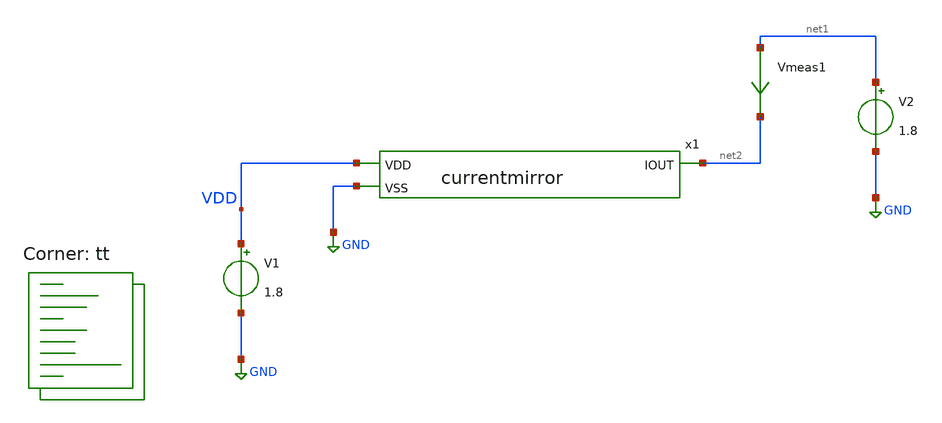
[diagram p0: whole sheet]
** sch_path: tt_um_upalermo_simple_analog_circuit/xschem/currentmirror_tb.sch
**.subckt currentmirror_tb
V2 net1 GND 1.8
V1 VDD GND 1.8
Vmeas1 net1 net2 0
.save i(vmeas1)
x1 VDD net2 GND currentmirror
**** begin user architecture code
.lib $::SKYWATER_MODELS/sky130.lib.spice tt


.control
.option savecurrents
dc V2 0 1.8 0.05
save all
plot i(vmeas1)
op
write currentmirror_tb.raw
.endc
.save all


**** end user architecture code
**.ends

* expanding   symbol:  Guido/TTSKY25A-UP-analog-circuit/xschem/currentmirror.sym # of pins=3
** sym_path: tt_um_upalermo_simple_analog_circuit/xschem/currentmirror.sym
** sch_path: tt_um_upalermo_simple_analog_circuit/xschem/currentmirror.sch
.subckt currentmirror VDD IOUT VSS
*.opin IOUT
*.ipin VSS
*.ipin VDD
XM1 net1 net1 VSS VSS sky130_fd_pr__nfet_01v8 L=5 W=10 nf=4 ad='int((nf+1)/2) * W/nf * 0.29' as='int((nf+2)/2) * W/nf * 0.29'
+ pd='2*int((nf+1)/2) * (W/nf + 0.29)' ps='2*int((nf+2)/2) * (W/nf + 0.29)' nrd='0.29 / W' nrs='0.29 / W'
+ sa=0 sb=0 sd=0 mult=1 m=1
XM2 IOUT net1 VSS VSS sky130_fd_pr__nfet_01v8 L=5 W=10 nf=4 ad='int((nf+1)/2) * W/nf * 0.29' as='int((nf+2)/2) * W/nf * 0.29'
+ pd='2*int((nf+1)/2) * (W/nf + 0.29)' ps='2*int((nf+2)/2) * (W/nf + 0.29)' nrd='0.29 / W' nrs='0.29 / W'
+ sa=0 sb=0 sd=0 mult=1 m=1
XR1 net1 net2 VSS sky130_fd_pr__res_high_po_0p35 L=15 mult=1 m=1
XR2 net2 net4 VSS sky130_fd_pr__res_high_po_0p35 L=15 mult=1 m=1
XR3 net4 net3 VSS sky130_fd_pr__res_high_po_0p35 L=15 mult=1 m=1
XR4 net3 VDD VSS sky130_fd_pr__res_high_po_0p35 L=15 mult=1 m=1
.ends

.GLOBAL GND
.end
